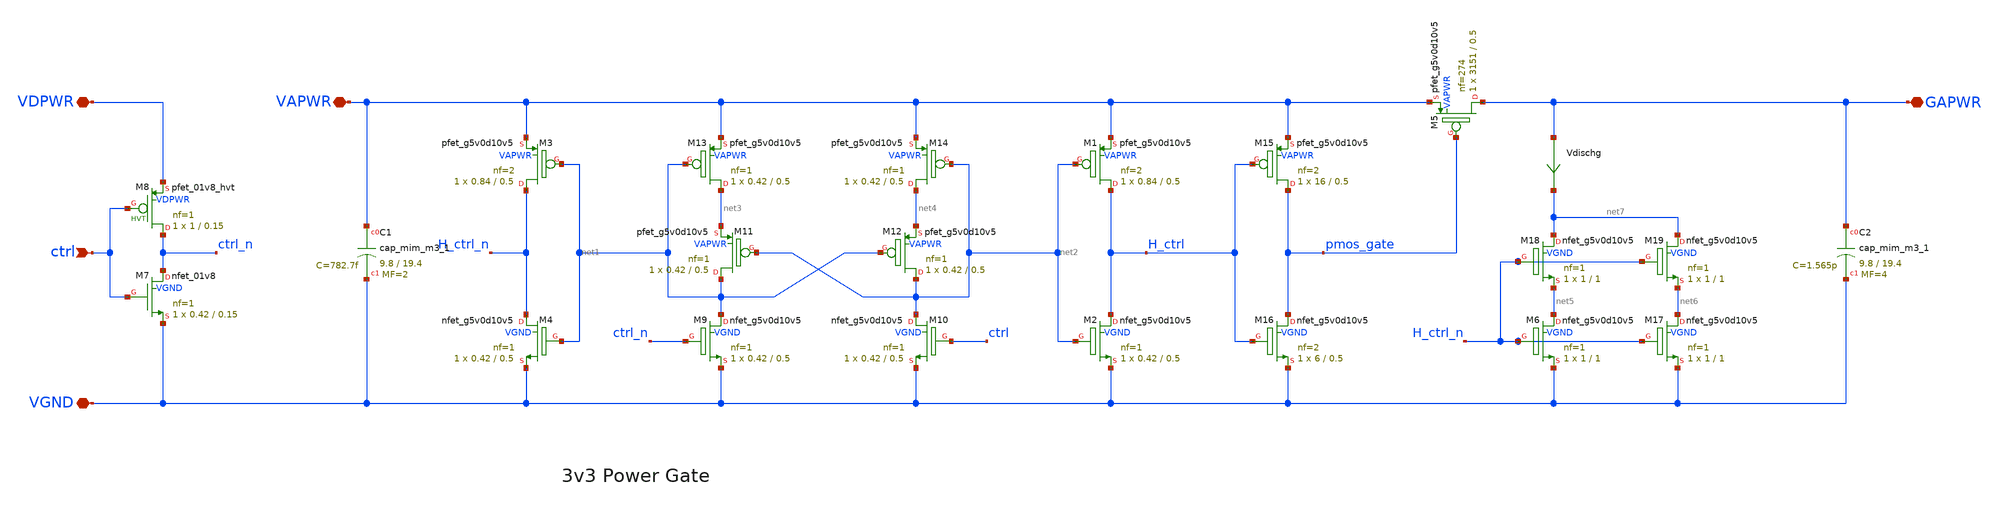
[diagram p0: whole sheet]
** sch_path: pg/sky130/tt_pg_3v3_2/xschem/tt_pg_3v3_2.sch
**.subckt tt_pg_3v3_2 GAPWR ctrl VGND VDPWR VAPWR
*.iopin GAPWR
*.ipin ctrl
*.iopin VGND
*.iopin VDPWR
*.iopin VAPWR
XM1 H_ctrl net2 VAPWR VAPWR sky130_fd_pr__pfet_g5v0d10v5 L=0.5 W=0.84 nf=2 ad='int((nf+1)/2) * W/nf * 0.29'
+ as='int((nf+2)/2) * W/nf * 0.29' pd='2*int((nf+1)/2) * (W/nf + 0.29)' ps='2*int((nf+2)/2) * (W/nf + 0.29)'
+ nrd='0.29 / W' nrs='0.29 / W' sa=0 sb=0 sd=0 mult=1 m=1
XM2 H_ctrl net2 VGND VGND sky130_fd_pr__nfet_g5v0d10v5 L=0.5 W=0.42 nf=1 ad='int((nf+1)/2) * W/nf * 0.29'
+ as='int((nf+2)/2) * W/nf * 0.29' pd='2*int((nf+1)/2) * (W/nf + 0.29)' ps='2*int((nf+2)/2) * (W/nf + 0.29)'
+ nrd='0.29 / W' nrs='0.29 / W' sa=0 sb=0 sd=0 mult=1 m=1
XM3 H_ctrl_n net1 VAPWR VAPWR sky130_fd_pr__pfet_g5v0d10v5 L=0.5 W=0.84 nf=2 ad='int((nf+1)/2) * W/nf * 0.29'
+ as='int((nf+2)/2) * W/nf * 0.29' pd='2*int((nf+1)/2) * (W/nf + 0.29)' ps='2*int((nf+2)/2) * (W/nf + 0.29)'
+ nrd='0.29 / W' nrs='0.29 / W' sa=0 sb=0 sd=0 mult=1 m=1
XM4 H_ctrl_n net1 VGND VGND sky130_fd_pr__nfet_g5v0d10v5 L=0.5 W=0.42 nf=1 ad='int((nf+1)/2) * W/nf * 0.29'
+ as='int((nf+2)/2) * W/nf * 0.29' pd='2*int((nf+1)/2) * (W/nf + 0.29)' ps='2*int((nf+2)/2) * (W/nf + 0.29)'
+ nrd='0.29 / W' nrs='0.29 / W' sa=0 sb=0 sd=0 mult=1 m=1
XM5 GAPWR pmos_gate VAPWR VAPWR sky130_fd_pr__pfet_g5v0d10v5 L=0.5 W=3151 nf=274 ad='int((nf+1)/2) * W/nf * 0.29'
+ as='int((nf+2)/2) * W/nf * 0.29' pd='2*int((nf+1)/2) * (W/nf + 0.29)' ps='2*int((nf+2)/2) * (W/nf + 0.29)'
+ nrd='0.29 / W' nrs='0.29 / W' sa=0 sb=0 sd=0 mult=1 m=1
XM7 ctrl_n ctrl VGND VGND sky130_fd_pr__nfet_01v8 L=0.15 W=0.42 nf=1 ad='int((nf+1)/2) * W/nf * 0.29'
+ as='int((nf+2)/2) * W/nf * 0.29' pd='2*int((nf+1)/2) * (W/nf + 0.29)' ps='2*int((nf+2)/2) * (W/nf + 0.29)'
+ nrd='0.29 / W' nrs='0.29 / W' sa=0 sb=0 sd=0 mult=1 m=1
XM8 ctrl_n ctrl VDPWR VDPWR sky130_fd_pr__pfet_01v8_hvt L=0.15 W=1 nf=1 ad='int((nf+1)/2) * W/nf * 0.29'
+ as='int((nf+2)/2) * W/nf * 0.29' pd='2*int((nf+1)/2) * (W/nf + 0.29)' ps='2*int((nf+2)/2) * (W/nf + 0.29)'
+ nrd='0.29 / W' nrs='0.29 / W' sa=0 sb=0 sd=0 mult=1 m=1
XM9 net1 ctrl_n VGND VGND sky130_fd_pr__nfet_g5v0d10v5 L=0.5 W=0.42 nf=1 ad='int((nf+1)/2) * W/nf * 0.29'
+ as='int((nf+2)/2) * W/nf * 0.29' pd='2*int((nf+1)/2) * (W/nf + 0.29)' ps='2*int((nf+2)/2) * (W/nf + 0.29)'
+ nrd='0.29 / W' nrs='0.29 / W' sa=0 sb=0 sd=0 mult=1 m=1
XM10 net2 ctrl VGND VGND sky130_fd_pr__nfet_g5v0d10v5 L=0.5 W=0.42 nf=1 ad='int((nf+1)/2) * W/nf * 0.29'
+ as='int((nf+2)/2) * W/nf * 0.29' pd='2*int((nf+1)/2) * (W/nf + 0.29)' ps='2*int((nf+2)/2) * (W/nf + 0.29)'
+ nrd='0.29 / W' nrs='0.29 / W' sa=0 sb=0 sd=0 mult=1 m=1
XM11 net1 net2 net3 VAPWR sky130_fd_pr__pfet_g5v0d10v5 L=0.5 W=0.42 nf=1 ad='int((nf+1)/2) * W/nf * 0.29'
+ as='int((nf+2)/2) * W/nf * 0.29' pd='2*int((nf+1)/2) * (W/nf + 0.29)' ps='2*int((nf+2)/2) * (W/nf + 0.29)'
+ nrd='0.29 / W' nrs='0.29 / W' sa=0 sb=0 sd=0 mult=1 m=1
XM12 net2 net1 net4 VAPWR sky130_fd_pr__pfet_g5v0d10v5 L=0.5 W=0.42 nf=1 ad='int((nf+1)/2) * W/nf * 0.29'
+ as='int((nf+2)/2) * W/nf * 0.29' pd='2*int((nf+1)/2) * (W/nf + 0.29)' ps='2*int((nf+2)/2) * (W/nf + 0.29)'
+ nrd='0.29 / W' nrs='0.29 / W' sa=0 sb=0 sd=0 mult=1 m=1
XM13 net3 net1 VAPWR VAPWR sky130_fd_pr__pfet_g5v0d10v5 L=0.5 W=0.42 nf=1 ad='int((nf+1)/2) * W/nf * 0.29'
+ as='int((nf+2)/2) * W/nf * 0.29' pd='2*int((nf+1)/2) * (W/nf + 0.29)' ps='2*int((nf+2)/2) * (W/nf + 0.29)'
+ nrd='0.29 / W' nrs='0.29 / W' sa=0 sb=0 sd=0 mult=1 m=1
XM14 net4 net2 VAPWR VAPWR sky130_fd_pr__pfet_g5v0d10v5 L=0.5 W=0.42 nf=1 ad='int((nf+1)/2) * W/nf * 0.29'
+ as='int((nf+2)/2) * W/nf * 0.29' pd='2*int((nf+1)/2) * (W/nf + 0.29)' ps='2*int((nf+2)/2) * (W/nf + 0.29)'
+ nrd='0.29 / W' nrs='0.29 / W' sa=0 sb=0 sd=0 mult=1 m=1
XM6 net5 H_ctrl_n VGND VGND sky130_fd_pr__nfet_g5v0d10v5 L=1 W=1 nf=1 ad='int((nf+1)/2) * W/nf * 0.29'
+ as='int((nf+2)/2) * W/nf * 0.29' pd='2*int((nf+1)/2) * (W/nf + 0.29)' ps='2*int((nf+2)/2) * (W/nf + 0.29)'
+ nrd='0.29 / W' nrs='0.29 / W' sa=0 sb=0 sd=0 mult=1 m=1
XC1 VAPWR VGND sky130_fd_pr__cap_mim_m3_1 W=9.8 L=19.4 MF=2 m=2
XC2 GAPWR VGND sky130_fd_pr__cap_mim_m3_1 W=9.8 L=19.4 MF=4 m=4
XM15 pmos_gate H_ctrl VAPWR VAPWR sky130_fd_pr__pfet_g5v0d10v5 L=0.5 W=16 nf=2 ad='int((nf+1)/2) * W/nf * 0.29'
+ as='int((nf+2)/2) * W/nf * 0.29' pd='2*int((nf+1)/2) * (W/nf + 0.29)' ps='2*int((nf+2)/2) * (W/nf + 0.29)'
+ nrd='0.29 / W' nrs='0.29 / W' sa=0 sb=0 sd=0 mult=1 m=1
XM16 pmos_gate H_ctrl VGND VGND sky130_fd_pr__nfet_g5v0d10v5 L=0.5 W=6 nf=2 ad='int((nf+1)/2) * W/nf * 0.29'
+ as='int((nf+2)/2) * W/nf * 0.29' pd='2*int((nf+1)/2) * (W/nf + 0.29)' ps='2*int((nf+2)/2) * (W/nf + 0.29)'
+ nrd='0.29 / W' nrs='0.29 / W' sa=0 sb=0 sd=0 mult=1 m=1
XM17 net6 H_ctrl_n VGND VGND sky130_fd_pr__nfet_g5v0d10v5 L=1 W=1 nf=1 ad='int((nf+1)/2) * W/nf * 0.29'
+ as='int((nf+2)/2) * W/nf * 0.29' pd='2*int((nf+1)/2) * (W/nf + 0.29)' ps='2*int((nf+2)/2) * (W/nf + 0.29)'
+ nrd='0.29 / W' nrs='0.29 / W' sa=0 sb=0 sd=0 mult=1 m=1
XM18 net7 H_ctrl_n net5 VGND sky130_fd_pr__nfet_g5v0d10v5 L=1 W=1 nf=1 ad='int((nf+1)/2) * W/nf * 0.29'
+ as='int((nf+2)/2) * W/nf * 0.29' pd='2*int((nf+1)/2) * (W/nf + 0.29)' ps='2*int((nf+2)/2) * (W/nf + 0.29)'
+ nrd='0.29 / W' nrs='0.29 / W' sa=0 sb=0 sd=0 mult=1 m=1
XM19 net7 H_ctrl_n net6 VGND sky130_fd_pr__nfet_g5v0d10v5 L=1 W=1 nf=1 ad='int((nf+1)/2) * W/nf * 0.29'
+ as='int((nf+2)/2) * W/nf * 0.29' pd='2*int((nf+1)/2) * (W/nf + 0.29)' ps='2*int((nf+2)/2) * (W/nf + 0.29)'
+ nrd='0.29 / W' nrs='0.29 / W' sa=0 sb=0 sd=0 mult=1 m=1
Vdischg GAPWR net7 0
.save i(vdischg)
**.ends
.end
